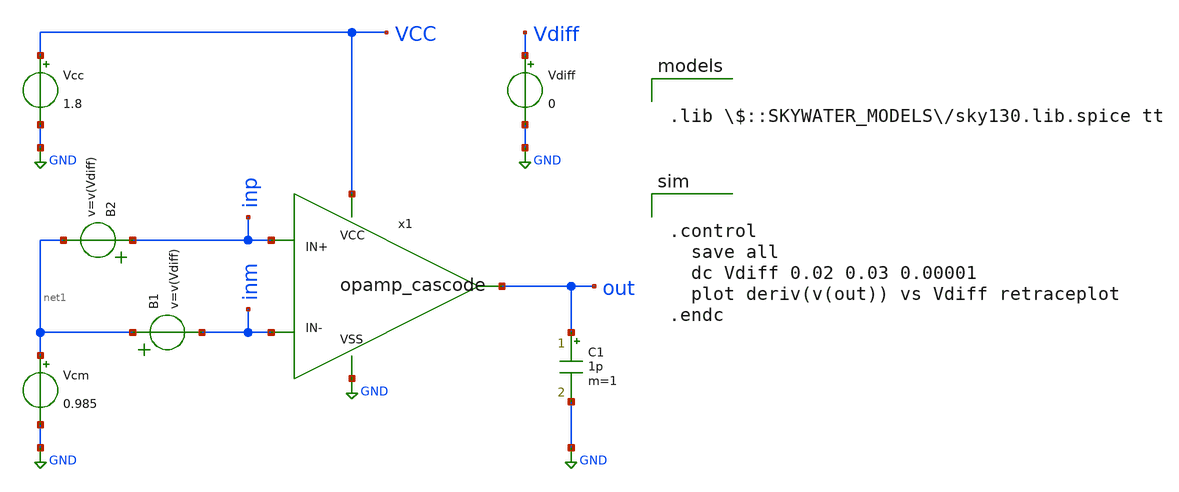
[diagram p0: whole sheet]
** sch_path: opamp_cascode_dc_sweep_10mV.sch
**.subckt opamp_cascode_dc_sweep_10mV
Vcc VCC GND 1.8
Vcm net1 GND 0.985
C1 out GND 1p m=1
x1 VCC GND inp inm out opamp_cascode
B1 net1 inm v=v(Vdiff)
Vdiff Vdiff GND 0
B2 inp net1 v=v(Vdiff)
**** begin user architecture code


.control
  save all
  dc Vdiff 0.02 0.03 0.00001
  plot deriv(v(out)) vs Vdiff retraceplot
.endc



.lib $::SKYWATER_MODELS/sky130.lib.spice tt

**** end user architecture code
**.ends

* expanding   symbol:  /home/zwierzak/projects/SKY130_OpAmp_GIT/opamp_cascode.sym # of pins=5
** sym_path: opamp_cascode.sym
** sch_path: opamp_cascode.sch
.subckt opamp_cascode VCC VSS IN+ IN- OUT
*.ipin IN+
*.ipin IN-
*.ipin VCC
*.ipin VSS
*.opin OUT
XM10 net8 net6 VCC VCC sky130_fd_pr__pfet_01v8 L=10 W=40 nf=1 ad='int((nf+1)/2) * W/nf * 0.29' as='int((nf+2)/2) * W/nf * 0.29'
+ pd='2*int((nf+1)/2) * (W/nf + 0.29)' ps='2*int((nf+2)/2) * (W/nf + 0.29)' nrd='0.29 / W' nrs='0.29 / W'
+ sa=0 sb=0 sd=0 mult=2 m=2
XM1 net7 net6 VCC VCC sky130_fd_pr__pfet_01v8 L=10 W=40 nf=1 ad='int((nf+1)/2) * W/nf * 0.29' as='int((nf+2)/2) * W/nf * 0.29'
+ pd='2*int((nf+1)/2) * (W/nf + 0.29)' ps='2*int((nf+2)/2) * (W/nf + 0.29)' nrd='0.29 / W' nrs='0.29 / W'
+ sa=0 sb=0 sd=0 mult=2 m=2
XM5 net3 net9 VCC VCC sky130_fd_pr__pfet_01v8 L=3 W=20 nf=1 ad='int((nf+1)/2) * W/nf * 0.29' as='int((nf+2)/2) * W/nf * 0.29'
+ pd='2*int((nf+1)/2) * (W/nf + 0.29)' ps='2*int((nf+2)/2) * (W/nf + 0.29)' nrd='0.29 / W' nrs='0.29 / W'
+ sa=0 sb=0 sd=0 mult=10 m=10
XM100 net9 net9 VCC VCC sky130_fd_pr__pfet_01v8 L=3 W=20 nf=1 ad='int((nf+1)/2) * W/nf * 0.29' as='int((nf+2)/2) * W/nf * 0.29'
+ pd='2*int((nf+1)/2) * (W/nf + 0.29)' ps='2*int((nf+2)/2) * (W/nf + 0.29)' nrd='0.29 / W' nrs='0.29 / W'
+ sa=0 sb=0 sd=0 mult=1 m=1
I0 net9 VSS 3.5u
XM11 OUT BIAS net8 net8 sky130_fd_pr__pfet_01v8 L=3 W=20 nf=1 ad='int((nf+1)/2) * W/nf * 0.29' as='int((nf+2)/2) * W/nf * 0.29'
+ pd='2*int((nf+1)/2) * (W/nf + 0.29)' ps='2*int((nf+2)/2) * (W/nf + 0.29)' nrd='0.29 / W' nrs='0.29 / W'
+ sa=0 sb=0 sd=0 mult=10 m=10
XM2 net6 BIAS net7 net7 sky130_fd_pr__pfet_01v8 L=3 W=20 nf=1 ad='int((nf+1)/2) * W/nf * 0.29' as='int((nf+2)/2) * W/nf * 0.29'
+ pd='2*int((nf+1)/2) * (W/nf + 0.29)' ps='2*int((nf+2)/2) * (W/nf + 0.29)' nrd='0.29 / W' nrs='0.29 / W'
+ sa=0 sb=0 sd=0 mult=10 m=10
XM6 net1 IN- net3 net3 sky130_fd_pr__pfet_01v8 L=0.25 W=25 nf=2 ad='int((nf+1)/2) * W/nf * 0.29' as='int((nf+2)/2) * W/nf * 0.29'
+ pd='2*int((nf+1)/2) * (W/nf + 0.29)' ps='2*int((nf+2)/2) * (W/nf + 0.29)' nrd='0.29 / W' nrs='0.29 / W'
+ sa=0 sb=0 sd=0 mult=3 m=3
XM8 net2 IN+ net3 net3 sky130_fd_pr__pfet_01v8 L=0.25 W=25 nf=2 ad='int((nf+1)/2) * W/nf * 0.29' as='int((nf+2)/2) * W/nf * 0.29'
+ pd='2*int((nf+1)/2) * (W/nf + 0.29)' ps='2*int((nf+2)/2) * (W/nf + 0.29)' nrd='0.29 / W' nrs='0.29 / W'
+ sa=0 sb=0 sd=0 mult=3 m=3
XM7 net1 net1 VSS VSS sky130_fd_pr__nfet_01v8 L=10 W=20 nf=1 ad='int((nf+1)/2) * W/nf * 0.29' as='int((nf+2)/2) * W/nf * 0.29'
+ pd='2*int((nf+1)/2) * (W/nf + 0.29)' ps='2*int((nf+2)/2) * (W/nf + 0.29)' nrd='0.29 / W' nrs='0.29 / W'
+ sa=0 sb=0 sd=0 mult=1 m=1
XM9 net2 net2 VSS VSS sky130_fd_pr__nfet_01v8 L=10 W=20 nf=1 ad='int((nf+1)/2) * W/nf * 0.29' as='int((nf+2)/2) * W/nf * 0.29'
+ pd='2*int((nf+1)/2) * (W/nf + 0.29)' ps='2*int((nf+2)/2) * (W/nf + 0.29)' nrd='0.29 / W' nrs='0.29 / W'
+ sa=0 sb=0 sd=0 mult=1 m=1
XM13 net4 net2 VSS VSS sky130_fd_pr__nfet_01v8 L=10 W=20 nf=1 ad='int((nf+1)/2) * W/nf * 0.29' as='int((nf+2)/2) * W/nf * 0.29'
+ pd='2*int((nf+1)/2) * (W/nf + 0.29)' ps='2*int((nf+2)/2) * (W/nf + 0.29)' nrd='0.29 / W' nrs='0.29 / W'
+ sa=0 sb=0 sd=0 mult=3 m=3
XM4 net5 net1 VSS VSS sky130_fd_pr__nfet_01v8 L=10 W=20 nf=1 ad='int((nf+1)/2) * W/nf * 0.29' as='int((nf+2)/2) * W/nf * 0.29'
+ pd='2*int((nf+1)/2) * (W/nf + 0.29)' ps='2*int((nf+2)/2) * (W/nf + 0.29)' nrd='0.29 / W' nrs='0.29 / W'
+ sa=0 sb=0 sd=0 mult=3 m=3
XM12 OUT BIAS1 net4 net4 sky130_fd_pr__nfet_01v8 L=3 W=20 nf=1 ad='int((nf+1)/2) * W/nf * 0.29' as='int((nf+2)/2) * W/nf * 0.29'
+ pd='2*int((nf+1)/2) * (W/nf + 0.29)' ps='2*int((nf+2)/2) * (W/nf + 0.29)' nrd='0.29 / W' nrs='0.29 / W'
+ sa=0 sb=0 sd=0 mult=5 m=5
XM3 net6 BIAS1 net5 net5 sky130_fd_pr__nfet_01v8 L=3 W=20 nf=1 ad='int((nf+1)/2) * W/nf * 0.29' as='int((nf+2)/2) * W/nf * 0.29'
+ pd='2*int((nf+1)/2) * (W/nf + 0.29)' ps='2*int((nf+2)/2) * (W/nf + 0.29)' nrd='0.29 / W' nrs='0.29 / W'
+ sa=0 sb=0 sd=0 mult=5 m=5
V1 BIAS VSS 0
V2 BIAS1 VSS 0.6
.ends

.GLOBAL GND
.end
